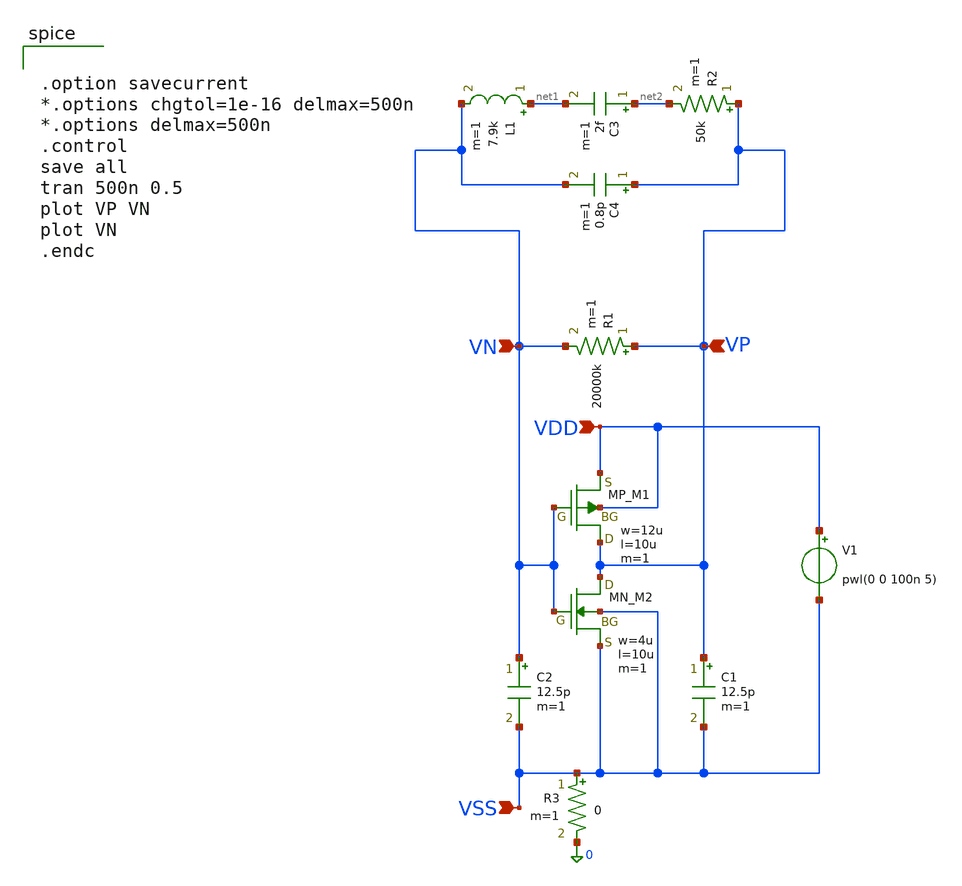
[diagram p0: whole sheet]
** sch_path: member_project/JJY_Receiver/Masahiro/jjy_recv/XTALOSC/XTALOSC.sch
**.subckt XTALOSC VSS VN VP VDD
*.ipin VSS
*.ipin VN
*.ipin VP
*.ipin VDD
R1 VP VN 20000k m=1
C1 VP VSS 12.5p m=1
C2 VN VSS 12.5p m=1
L1 net1 VN 7.9k m=1
C3 net2 net1 2f m=1
R2 VP net2 50k m=1
C4 VP VN 0.8p m=1
V1 VDD VSS pwl(0 0 100n 5)
R3 VSS 0 0 m=1
XM1 VP VN VDD VDD PMOS w=12u l=10u as=0 ad=0 ps=0 pd=0 nrd=0 nrs=0 m=1
XM2 VP VN VSS VSS NMOS w=4u l=10u as=0 ad=0 ps=0 pd=0 nrd=0 nrs=0 m=1
**** begin user architecture code
 .include $::LIB/ip62_models


.option savecurrent
*.options chgtol=1e-16 delmax=500n
*.options delmax=500n
.control
save all
tran 500n 0.5
plot VP VN
plot VN
.endc


**** end user architecture code
**.ends
.end
